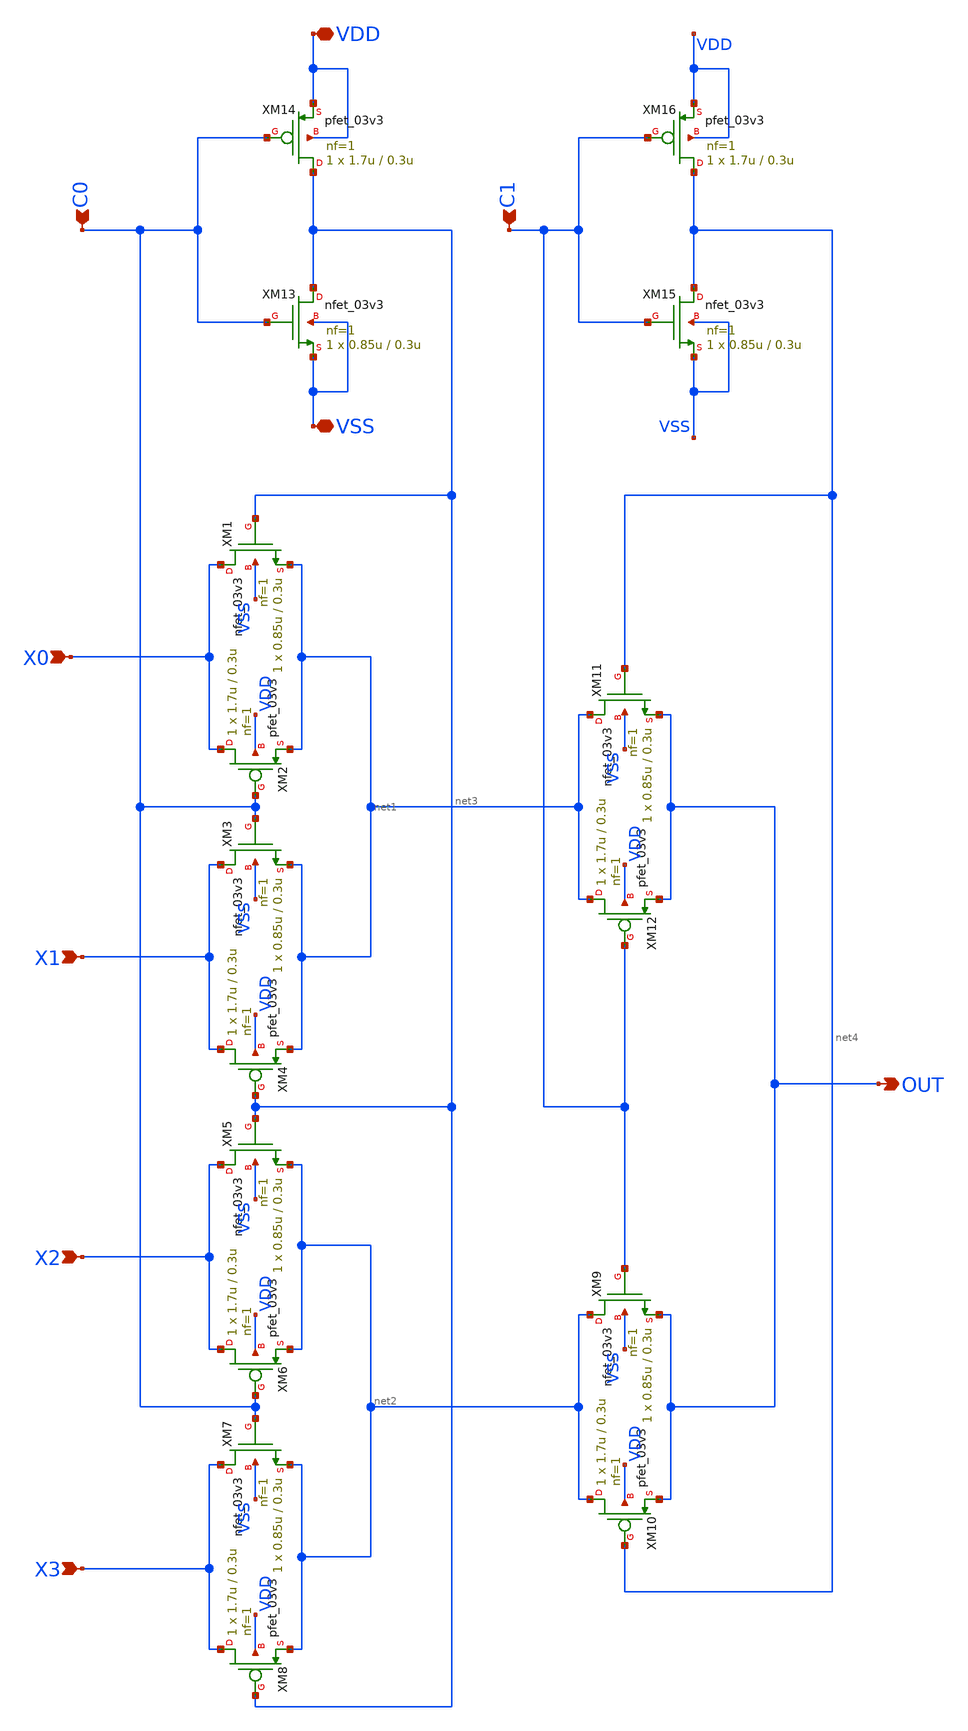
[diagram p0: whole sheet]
** sch_path: designs/MUX4/Pre_Layout/Schematic/gf180mcu_osu_sc_gp9t3v3__mux4_1.sch
**.subckt gf180mcu_osu_sc_gp9t3v3__mux4_1 X0 X1 X2 X3 C0 C1 OUT VDD VSS
*.ipin X0
*.ipin X1
*.ipin X2
*.ipin X3
*.ipin C0
*.ipin C1
*.opin OUT
*.iopin VDD
*.iopin VSS
XM1 X0 net3 net1 VSS nfet_03v3 L=0.3u W=0.85u nf=1 ad='int((nf+1)/2) * W/nf * 0.18u' as='int((nf+2)/2) * W/nf * 0.18u'
+ pd='2*int((nf+1)/2) * (W/nf + 0.18u)' ps='2*int((nf+2)/2) * (W/nf + 0.18u)' nrd='0.18u / W' nrs='0.18u / W'
+ sa=0 sb=0 sd=0 m=1
XM2 X0 C0 net1 VDD pfet_03v3 L=0.3u W=1.7u nf=1 ad='int((nf+1)/2) * W/nf * 0.18u' as='int((nf+2)/2) * W/nf * 0.18u'
+ pd='2*int((nf+1)/2) * (W/nf + 0.18u)' ps='2*int((nf+2)/2) * (W/nf + 0.18u)' nrd='0.18u / W' nrs='0.18u / W'
+ sa=0 sb=0 sd=0 m=1
XM3 X1 C0 net1 VSS nfet_03v3 L=0.3u W=0.85u nf=1 ad='int((nf+1)/2) * W/nf * 0.18u' as='int((nf+2)/2) * W/nf * 0.18u'
+ pd='2*int((nf+1)/2) * (W/nf + 0.18u)' ps='2*int((nf+2)/2) * (W/nf + 0.18u)' nrd='0.18u / W' nrs='0.18u / W'
+ sa=0 sb=0 sd=0 m=1
XM5 X2 net3 net2 VSS nfet_03v3 L=0.3u W=0.85u nf=1 ad='int((nf+1)/2) * W/nf * 0.18u' as='int((nf+2)/2) * W/nf * 0.18u'
+ pd='2*int((nf+1)/2) * (W/nf + 0.18u)' ps='2*int((nf+2)/2) * (W/nf + 0.18u)' nrd='0.18u / W' nrs='0.18u / W'
+ sa=0 sb=0 sd=0 m=1
XM7 X3 C0 net2 VSS nfet_03v3 L=0.3u W=0.85u nf=1 ad='int((nf+1)/2) * W/nf * 0.18u' as='int((nf+2)/2) * W/nf * 0.18u'
+ pd='2*int((nf+1)/2) * (W/nf + 0.18u)' ps='2*int((nf+2)/2) * (W/nf + 0.18u)' nrd='0.18u / W' nrs='0.18u / W'
+ sa=0 sb=0 sd=0 m=1
XM9 net2 C1 OUT VSS nfet_03v3 L=0.3u W=0.85u nf=1 ad='int((nf+1)/2) * W/nf * 0.18u' as='int((nf+2)/2) * W/nf * 0.18u'
+ pd='2*int((nf+1)/2) * (W/nf + 0.18u)' ps='2*int((nf+2)/2) * (W/nf + 0.18u)' nrd='0.18u / W' nrs='0.18u / W'
+ sa=0 sb=0 sd=0 m=1
XM11 net1 net4 OUT VSS nfet_03v3 L=0.3u W=0.85u nf=1 ad='int((nf+1)/2) * W/nf * 0.18u' as='int((nf+2)/2) * W/nf * 0.18u'
+ pd='2*int((nf+1)/2) * (W/nf + 0.18u)' ps='2*int((nf+2)/2) * (W/nf + 0.18u)' nrd='0.18u / W' nrs='0.18u / W'
+ sa=0 sb=0 sd=0 m=1
XM4 X1 net3 net1 VDD pfet_03v3 L=0.3u W=1.7u nf=1 ad='int((nf+1)/2) * W/nf * 0.18u' as='int((nf+2)/2) * W/nf * 0.18u'
+ pd='2*int((nf+1)/2) * (W/nf + 0.18u)' ps='2*int((nf+2)/2) * (W/nf + 0.18u)' nrd='0.18u / W' nrs='0.18u / W'
+ sa=0 sb=0 sd=0 m=1
XM6 X2 C0 net2 VDD pfet_03v3 L=0.3u W=1.7u nf=1 ad='int((nf+1)/2) * W/nf * 0.18u' as='int((nf+2)/2) * W/nf * 0.18u'
+ pd='2*int((nf+1)/2) * (W/nf + 0.18u)' ps='2*int((nf+2)/2) * (W/nf + 0.18u)' nrd='0.18u / W' nrs='0.18u / W'
+ sa=0 sb=0 sd=0 m=1
XM8 X3 net3 net2 VDD pfet_03v3 L=0.3u W=1.7u nf=1 ad='int((nf+1)/2) * W/nf * 0.18u' as='int((nf+2)/2) * W/nf * 0.18u'
+ pd='2*int((nf+1)/2) * (W/nf + 0.18u)' ps='2*int((nf+2)/2) * (W/nf + 0.18u)' nrd='0.18u / W' nrs='0.18u / W'
+ sa=0 sb=0 sd=0 m=1
XM10 net2 net4 OUT VDD pfet_03v3 L=0.3u W=1.7u nf=1 ad='int((nf+1)/2) * W/nf * 0.18u' as='int((nf+2)/2) * W/nf * 0.18u'
+ pd='2*int((nf+1)/2) * (W/nf + 0.18u)' ps='2*int((nf+2)/2) * (W/nf + 0.18u)' nrd='0.18u / W' nrs='0.18u / W'
+ sa=0 sb=0 sd=0 m=1
XM12 net1 C1 OUT VDD pfet_03v3 L=0.3u W=1.7u nf=1 ad='int((nf+1)/2) * W/nf * 0.18u' as='int((nf+2)/2) * W/nf * 0.18u'
+ pd='2*int((nf+1)/2) * (W/nf + 0.18u)' ps='2*int((nf+2)/2) * (W/nf + 0.18u)' nrd='0.18u / W' nrs='0.18u / W'
+ sa=0 sb=0 sd=0 m=1
XM13 net3 C0 VSS VSS nfet_03v3 L=0.3u W=0.85u nf=1 ad='int((nf+1)/2) * W/nf * 0.18u' as='int((nf+2)/2) * W/nf * 0.18u'
+ pd='2*int((nf+1)/2) * (W/nf + 0.18u)' ps='2*int((nf+2)/2) * (W/nf + 0.18u)' nrd='0.18u / W' nrs='0.18u / W'
+ sa=0 sb=0 sd=0 m=1
XM14 net3 C0 VDD VDD pfet_03v3 L=0.3u W=1.7u nf=1 ad='int((nf+1)/2) * W/nf * 0.18u' as='int((nf+2)/2) * W/nf * 0.18u'
+ pd='2*int((nf+1)/2) * (W/nf + 0.18u)' ps='2*int((nf+2)/2) * (W/nf + 0.18u)' nrd='0.18u / W' nrs='0.18u / W'
+ sa=0 sb=0 sd=0 m=1
XM15 net4 C1 VSS VSS nfet_03v3 L=0.3u W=0.85u nf=1 ad='int((nf+1)/2) * W/nf * 0.18u' as='int((nf+2)/2) * W/nf * 0.18u'
+ pd='2*int((nf+1)/2) * (W/nf + 0.18u)' ps='2*int((nf+2)/2) * (W/nf + 0.18u)' nrd='0.18u / W' nrs='0.18u / W'
+ sa=0 sb=0 sd=0 m=1
XM16 net4 C1 VDD VDD pfet_03v3 L=0.3u W=1.7u nf=1 ad='int((nf+1)/2) * W/nf * 0.18u' as='int((nf+2)/2) * W/nf * 0.18u'
+ pd='2*int((nf+1)/2) * (W/nf + 0.18u)' ps='2*int((nf+2)/2) * (W/nf + 0.18u)' nrd='0.18u / W' nrs='0.18u / W'
+ sa=0 sb=0 sd=0 m=1
**.ends
.end
